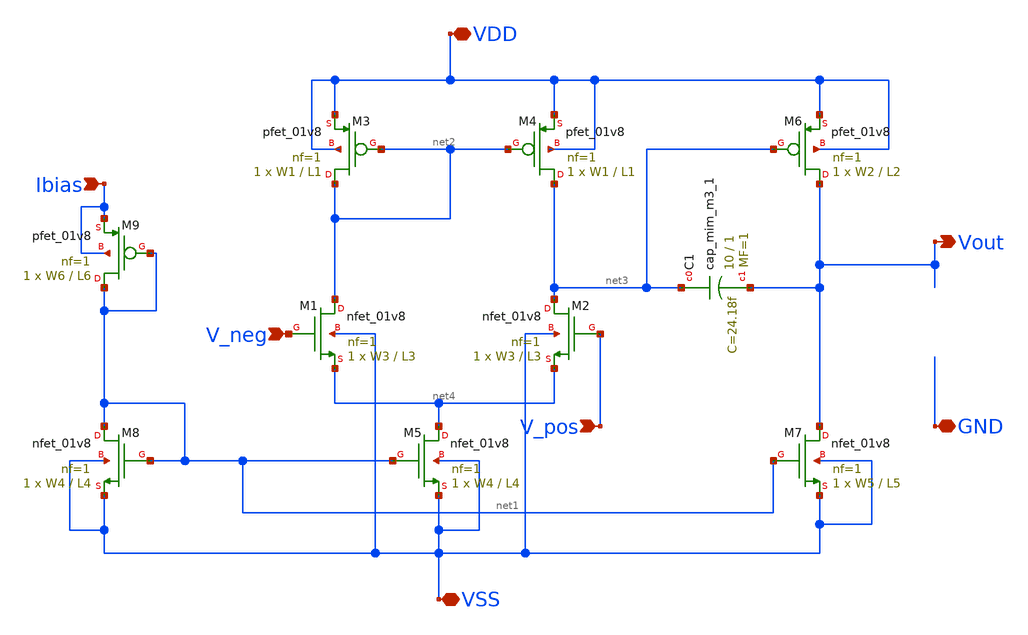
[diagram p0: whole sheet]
** sch_path: two_stage_opamp/two_stage_opamp.sch
**.subckt two_stage_opamp Ibias V_neg V_pos VDD VSS Vout GND
*.ipin Ibias
*.ipin V_neg
*.ipin V_pos
*.iopin VDD
*.iopin VSS
*.opin Vout
*.iopin GND
XM1 net2 V_neg net4 VSS sky130_fd_pr__nfet_01v8 L=L3 W=W3 nf=1 ad='int((nf+1)/2) * W/nf * 0.29' as='int((nf+2)/2) * W/nf * 0.29'
+ pd='2*int((nf+1)/2) * (W/nf + 0.29)' ps='2*int((nf+2)/2) * (W/nf + 0.29)' nrd='0.29 / W' nrs='0.29 / W'
+ sa=0 sb=0 sd=0 mult=1 m=1
XM3 net2 net2 VDD VDD sky130_fd_pr__pfet_01v8 L=L1 W=W1 nf=1 ad='int((nf+1)/2) * W/nf * 0.29' as='int((nf+2)/2) * W/nf * 0.29'
+ pd='2*int((nf+1)/2) * (W/nf + 0.29)' ps='2*int((nf+2)/2) * (W/nf + 0.29)' nrd='0.29 / W' nrs='0.29 / W'
+ sa=0 sb=0 sd=0 mult=1 m=1
XM2 net3 V_pos net4 VSS sky130_fd_pr__nfet_01v8 L=L3 W=W3 nf=1 ad='int((nf+1)/2) * W/nf * 0.29' as='int((nf+2)/2) * W/nf * 0.29'
+ pd='2*int((nf+1)/2) * (W/nf + 0.29)' ps='2*int((nf+2)/2) * (W/nf + 0.29)' nrd='0.29 / W' nrs='0.29 / W'
+ sa=0 sb=0 sd=0 mult=1 m=1
XM4 net3 net2 VDD VDD sky130_fd_pr__pfet_01v8 L=L1 W=W1 nf=1 ad='int((nf+1)/2) * W/nf * 0.29' as='int((nf+2)/2) * W/nf * 0.29'
+ pd='2*int((nf+1)/2) * (W/nf + 0.29)' ps='2*int((nf+2)/2) * (W/nf + 0.29)' nrd='0.29 / W' nrs='0.29 / W'
+ sa=0 sb=0 sd=0 mult=1 m=1
XM5 net4 net1 VSS VSS sky130_fd_pr__nfet_01v8 L=L4 W=W4 nf=1 ad='int((nf+1)/2) * W/nf * 0.29' as='int((nf+2)/2) * W/nf * 0.29'
+ pd='2*int((nf+1)/2) * (W/nf + 0.29)' ps='2*int((nf+2)/2) * (W/nf + 0.29)' nrd='0.29 / W' nrs='0.29 / W'
+ sa=0 sb=0 sd=0 mult=1 m=1
XM6 Vout net3 VDD VDD sky130_fd_pr__pfet_01v8 L=L2 W=W2 nf=1 ad='int((nf+1)/2) * W/nf * 0.29' as='int((nf+2)/2) * W/nf * 0.29'
+ pd='2*int((nf+1)/2) * (W/nf + 0.29)' ps='2*int((nf+2)/2) * (W/nf + 0.29)' nrd='0.29 / W' nrs='0.29 / W'
+ sa=0 sb=0 sd=0 mult=1 m=1
XM7 Vout net1 VSS VSS sky130_fd_pr__nfet_01v8 L=L5 W=W5 nf=1 ad='int((nf+1)/2) * W/nf * 0.29' as='int((nf+2)/2) * W/nf * 0.29'
+ pd='2*int((nf+1)/2) * (W/nf + 0.29)' ps='2*int((nf+2)/2) * (W/nf + 0.29)' nrd='0.29 / W' nrs='0.29 / W'
+ sa=0 sb=0 sd=0 mult=1 m=1
XM8 net1 net1 VSS VSS sky130_fd_pr__nfet_01v8 L=L4 W=W4 nf=1 ad='int((nf+1)/2) * W/nf * 0.29' as='int((nf+2)/2) * W/nf * 0.29'
+ pd='2*int((nf+1)/2) * (W/nf + 0.29)' ps='2*int((nf+2)/2) * (W/nf + 0.29)' nrd='0.29 / W' nrs='0.29 / W'
+ sa=0 sb=0 sd=0 mult=1 m=1
XM9 net1 net1 Ibias Ibias sky130_fd_pr__pfet_01v8 L=L6 W=W6 nf=1 ad='int((nf+1)/2) * W/nf * 0.29' as='int((nf+2)/2) * W/nf * 0.29'
+ pd='2*int((nf+1)/2) * (W/nf + 0.29)' ps='2*int((nf+2)/2) * (W/nf + 0.29)' nrd='0.29 / W' nrs='0.29 / W'
+ sa=0 sb=0 sd=0 mult=1 m=1
XC1 net3 Vout sky130_fd_pr__cap_mim_m3_1 W=10 L=1 MF=1 m=1
**.ends
.end
